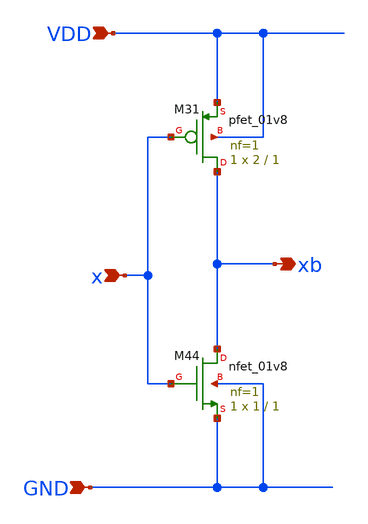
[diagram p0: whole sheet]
** sch_path: xschem/inverter.sch
**.subckt inverter VDD GND xb x
*.ipin VDD
*.ipin GND
*.opin xb
*.ipin x
XM31 xb x VDD VDD sky130_fd_pr__pfet_01v8 L=1 W=2 nf=1 ad='int((nf+1)/2) * W/nf * 0.29' as='int((nf+2)/2) * W/nf * 0.29'
+ pd='2*int((nf+1)/2) * (W/nf + 0.29)' ps='2*int((nf+2)/2) * (W/nf + 0.29)' nrd='0.29 / W' nrs='0.29 / W'
+ sa=0 sb=0 sd=0 mult=1 m=1
XM44 xb x GND GND sky130_fd_pr__nfet_01v8 L=1 W=1 nf=1 ad='int((nf+1)/2) * W/nf * 0.29' as='int((nf+2)/2) * W/nf * 0.29'
+ pd='2*int((nf+1)/2) * (W/nf + 0.29)' ps='2*int((nf+2)/2) * (W/nf + 0.29)' nrd='0.29 / W' nrs='0.29 / W'
+ sa=0 sb=0 sd=0 mult=1 m=1
**.ends
.end
